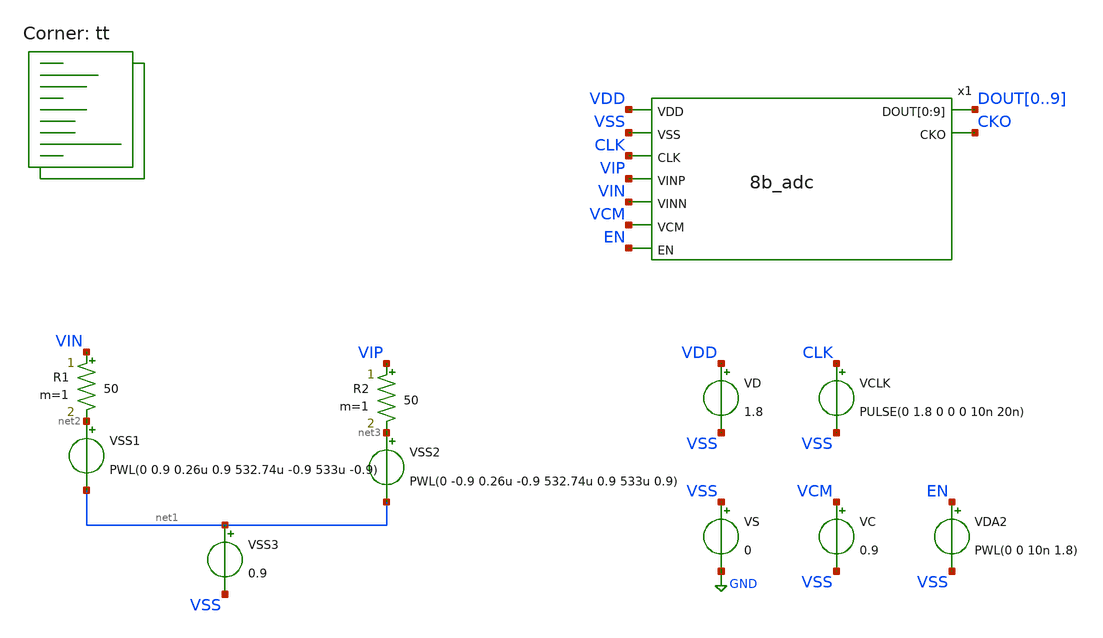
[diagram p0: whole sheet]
** sch_path: xschem/adc_tb_static.sch
**.subckt adc_tb_static
VS VSS GND 0
VD VDD VSS 1.8
x1 VDD VSS CLK VIP VIN VCM EN DOUT0 DOUT1 DOUT2 DOUT3 DOUT4 DOUT5 DOUT6 DOUT7 DOUT8 DOUT9 CKO 8b_adc
VC VCM VSS 0.9
VDA2 EN VSS PWL(0 0 10n 1.8)
VSS1 net2 net1 PWL(0 0.9 0.26u 0.9 532.74u -0.9 533u -0.9)
VSS2 net3 net1 PWL(0 -0.9 0.26u -0.9 532.74u 0.9 533u 0.9)
VSS3 net1 VSS 0.9
R1 VIN net2 50 m=1
R2 VIP net3 50 m=1
VCLK CLK VSS PULSE(0 1.8 0 0 0 10n 20n)
**** begin user architecture code

** opencircuitdesign pdks install
* .lib $::SKYWATER_MODELS/sky130.lib.spice tt
.include $PDK_ROOT/$PDK/libs.ref/sky130_fd_sc_hd/spice/sky130_fd_sc_hd.spice



.option wnflag=0 bypass=1
.options method=gear reltol=1e-5 rawfile=binary
.options solver=klu nomod
.control
global netlist_dir .
set num_threads=32
set wr_singlescale
save x1.vcp x1.vcn vip vin clk vcm cko x1.cks x1.cksb vdd i(vd)  dout0 dout1 dout2 dout3 dout4 dout5
+ dout6 dout7 dout8 dout9
tran 1n 535u 0 1n uic ; Mengubah start time menjadi 10n
rusage traniter trantime
let pow = -i(vd)*vdd
meas tran inst_pow MAX pow from=1n to=535u
meas tran avg_pow  AVG pow from=1n to=535u
remzerovec
write adc10b_tb_static.raw
wrdata adc10b_tb_static.txt cko dout0 dout1 dout2 dout3 dout4 dout5 dout6 dout7 dout8 dout9 pow
quit 1
.endc


.lib $::SKYWATER_MODELS/sky130.lib.spice tt
**** end user architecture code
**.ends
.GLOBAL GND
.end
